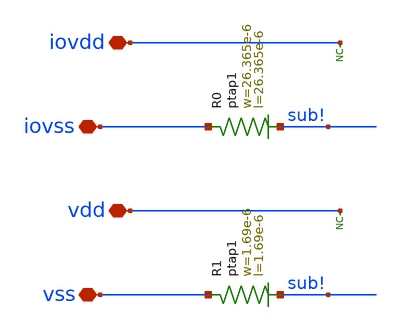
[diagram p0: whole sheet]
** sch_path: ihp-sg13g2/libs.ref/sg13g2_io/sch/xschem/sg13g2_Filler2000.sch
**.subckt sg13g2_Filler2000 iovdd iovss vdd vss
*.iopin iovdd
*.iopin iovss
*.iopin vdd
*.iopin vss
* noconn iovdd
* noconn vdd
XR0 iovss sub! ptap1 R=1.224 w=26.365e-6 l=26.365e-6
XR1 vss sub! ptap1 R=101.9 w=1.69e-6 l=1.69e-6
**.ends
.end
